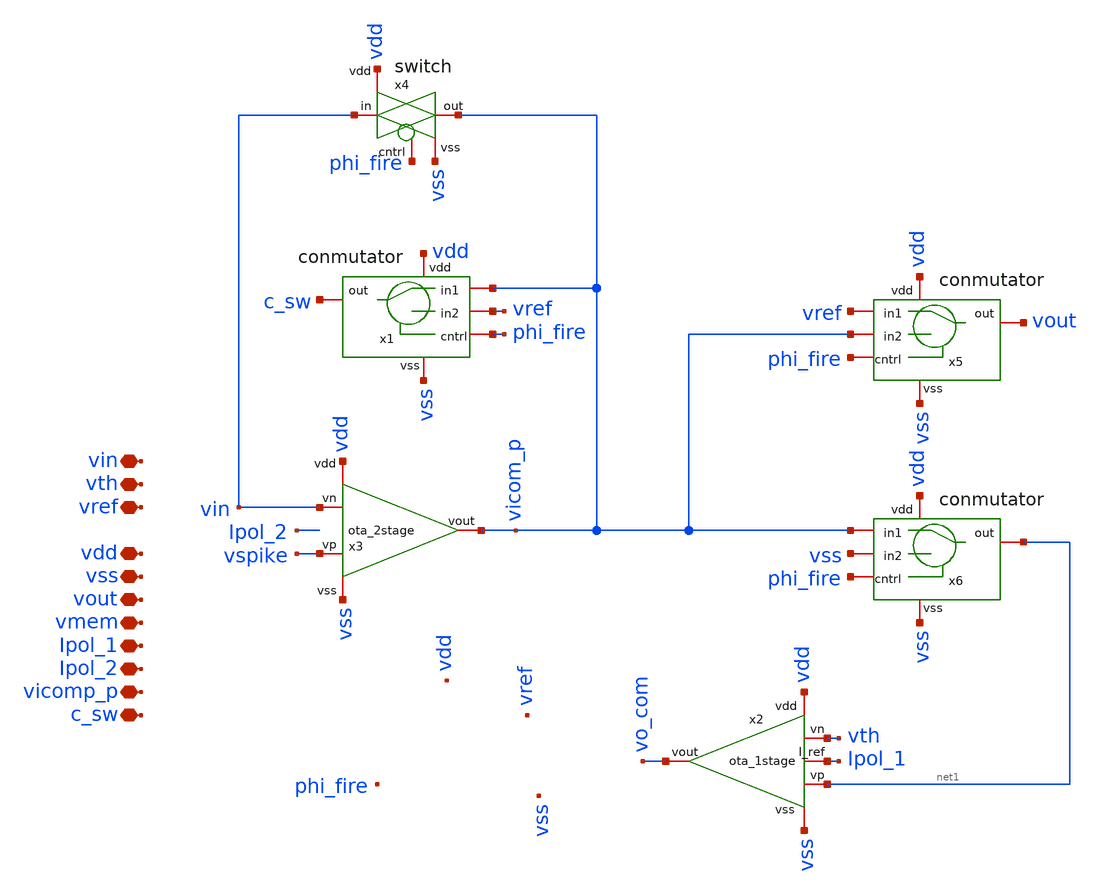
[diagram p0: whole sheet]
** sch_path: designs/libs/core_LIF_comp/LIF_comp.sch
**.subckt LIF_comp vin vth vref vdd vss vout vmem Ipol_1 vicomp_p c_sw Ipol_2
*.iopin vin
*.iopin vth
*.iopin vref
*.iopin vdd
*.iopin vss
*.iopin vout
*.iopin vmem
*.iopin Ipol_1
*.iopin vicomp_p
*.iopin c_sw
*.iopin Ipol_2
x1 phi_fire vdd vref c_sw vicom_p vss conmutator
x2 vdd vo_com net1 vth Ipol_1 vss ota_1stage
x3 vdd vin vicom_p vspike vss ota_2stage
x4 vdd vin vicom_p phi_fire vss switch
x5 phi_fire vdd vicom_p vout vref vss conmutator
x6 phi_fire vdd vss net1 vicom_p vss conmutator
**.ends
.end
